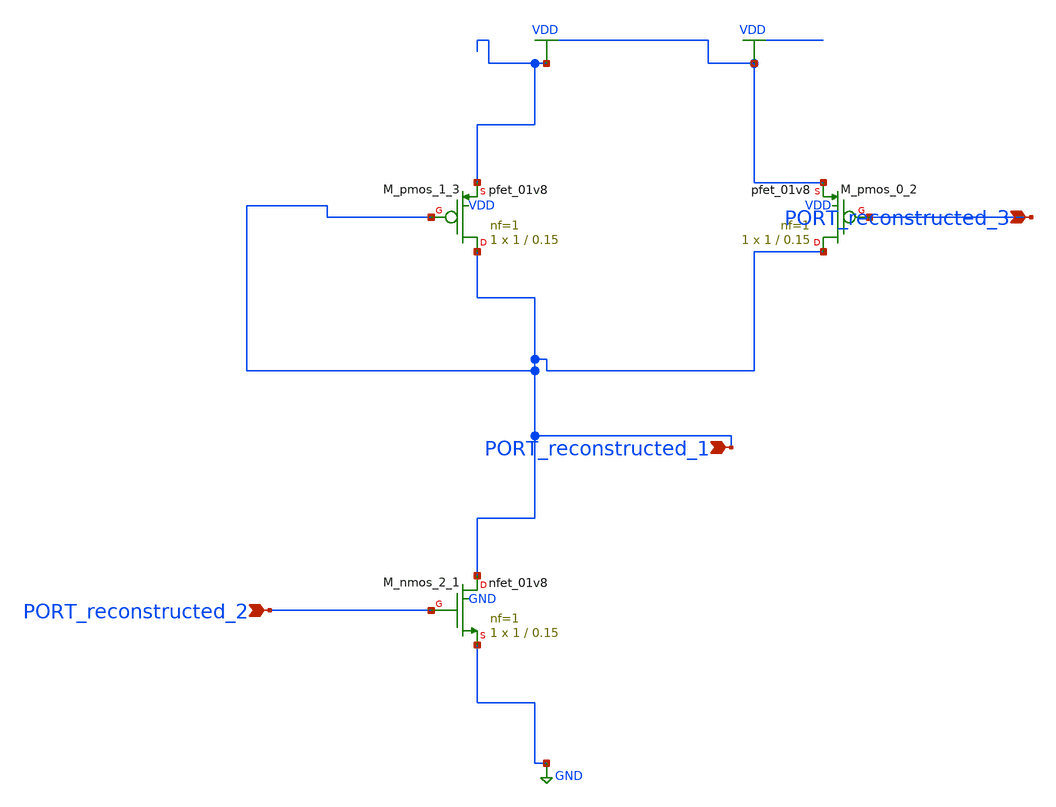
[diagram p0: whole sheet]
** sch_path: schematics/AMSNet/253.sch
**.subckt 253 PORT_reconstructed_2 PORT_reconstructed_3 PORT_reconstructed_1
*.ipin PORT_reconstructed_2
*.ipin PORT_reconstructed_3
*.ipin PORT_reconstructed_1
XM_nmos_2_1 PORT_reconstructed_1 PORT_reconstructed_2 GND GND sky130_fd_pr__nfet_01v8 L=0.15 W=1 nf=1
+ ad='int((1 + 1)/2) * 1 / 1 * 0.29' as='int((1 + 2)/2) * 1 / 1 * 0.29' pd='2*int((1 + 1)/2) * (1 / 1 + 0.29)'
+ ps='2*int((1 + 2)/2) * (1 / 1 + 0.29)' nrd='0.29 / 1 ' nrs='0.29 / 1 ' sa=0 sb=0 sd=0 mult=1 m=1
XM_pmos_0_2 PORT_reconstructed_1 PORT_reconstructed_3 VDD VDD sky130_fd_pr__pfet_01v8 L=0.15 W=1 nf=1
+ ad='int((1 + 1)/2) * 1 / 1 * 0.29' as='int((1 + 2)/2) * 1 / 1 * 0.29' pd='2*int((1 + 1)/2) * (1 / 1 + 0.29)'
+ ps='2*int((1 + 2)/2) * (1 / 1 + 0.29)' nrd='0.29 / 1 ' nrs='0.29 / 1 ' sa=0 sb=0 sd=0 mult=1 m=1
XM_pmos_1_3 PORT_reconstructed_1 PORT_reconstructed_1 VDD VDD sky130_fd_pr__pfet_01v8 L=0.15 W=1 nf=1
+ ad='int((1 + 1)/2) * 1 / 1 * 0.29' as='int((1 + 2)/2) * 1 / 1 * 0.29' pd='2*int((1 + 1)/2) * (1 / 1 + 0.29)'
+ ps='2*int((1 + 2)/2) * (1 / 1 + 0.29)' nrd='0.29 / 1 ' nrs='0.29 / 1 ' sa=0 sb=0 sd=0 mult=1 m=1
**.ends
.GLOBAL GND
.GLOBAL VDD
.end
